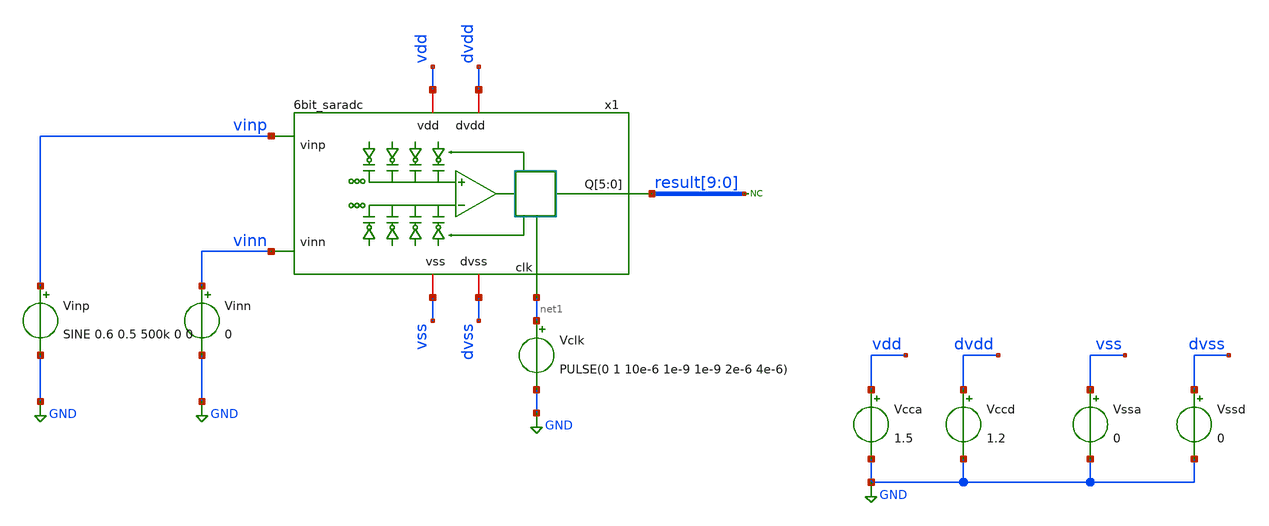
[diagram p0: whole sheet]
** sch_path: xschem/adc/tb_adc.sch
**.subckt tb_adc
x1 vdd vss dvdd dvss result[9] result[8] result[7] result[6] result[5] result[4] vinn net1 vinp
+ 6bit_saradc
Vclk net1 GND PULSE(0 1 10e-6 1e-9 1e-9 2e-6 4e-6)
Vssa vss GND 0
Vcca vdd GND 1.5
Vssd dvss GND 0
Vccd dvdd GND 1.2
Vinn vinn GND 0
Vinp vinp GND SINE 0.6 0.5 500k 0 0
* noconn result[9:0]
**** begin user architecture code

.lib $::SKYWATER_MODELS/models/sky130.lib.spice tt
.include $::SKYWATER_STDCELLS/cells/inv/sky130_fd_sc_hd__inv_4.spice
.include $::SKYWATER_STDCELLS/cells/decap/sky130_fd_sc_hd__decap_8.spice
.include $::SKYWATER_STDCELLS/cells/decap/sky130_fd_sc_hd__decap_3.spice
.include $::SKYWATER_STDCELLS/cells/buf/sky130_fd_sc_hd__buf_1.spice
.include $::SKYWATER_STDCELLS/cells/inv/sky130_fd_sc_hd__inv_1.spice
.include $::SKYWATER_STDCELLS/cells/inv/sky130_fd_sc_hd__inv_2.spice
.include $::SKYWATER_STDCELLS/cells/nor2/sky130_fd_sc_hd__nor2_1.spice
.include $::SKYWATER_STDCELLS/cells/or3/sky130_fd_sc_hd__or3_1.spice
.include $::SKYWATER_STDCELLS/cells/and2/sky130_fd_sc_hd__and2_0.spice
.include $::SKYWATER_STDCELLS/cells/dfrbp/sky130_fd_sc_hd__dfrbp_1.spice
.include $::SKYWATER_STDCELLS/cells/tap/sky130_fd_sc_hd__tap_2.spice

 *-------------------------
* normal setup
*-------------------------
.options method = gear
.options gmin   = 1e-15
.options abstol = 1e-14
.options chtol  = 1e-18
.options reltol = 100e-6
*-------------------------

*-------------------------
* extracted logic setup
*-------------------------
*.options method = gear
*.options gmin   = 1e-12
*.options abstol = 1e-10
*.options chtol  = 1e-12
*.options reltol = 100e-3
*-------------------------



*.include $::DESIGN_PATH/switches/bootstrapped_sw.sp
*.include $::DESIGN_PATH/sar_10b/dac/dac_mom.pex.sp
*.include $::DESIGN_PATH/sar_10b/sar/sar.pex.spice
*.include $::DESIGN_PATH/sar_10b/sar/sar_mom.pex.spice
*.include $::DESIGN_PATH/sar_10b/sar/sar_mim.pex.spice
*.include $::DESIGN_PATH/sar_10b/control/sarlogic.ext.spice
*.include $::DESIGN_PATH/sar_10b/sar/sar.pex.spice
*.include $::DESIGN_PATH/sar_10b/sar/sar.ext.spice

.param MC_SWITCH=0
.param vin=0.1
.param vcm=0.75
.param vsigp=vcm + vin/2
.param vsign=vcm - vin/2

.tran 100e-9 10e-6 uic

.control

run

.endc

 * FET CORNERS
*.include $::SKYWATER_MODELS/corners/tt_all.spice
*.include $::SKYWATER_MODELS/corners/ff_all.spice
*.include $::SKYWATER_MODELS/corners/ss_all.spice
*.include $::SKYWATER_MODELS/corners/tt.spice
*.include $::SKYWATER_MODELS/corners/ff.spice
*.include $::SKYWATER_MODELS/corners/ss.spice
*.include $::SKYWATER_MODELS/corners/sf.spice
*.include $::SKYWATER_MODELS/corners/fs.spice

* TT + R + C
*.include $::SKYWATER_MODELS/corners/tt_rmax_cmax.spice
*.include $::SKYWATER_MODELS/corners/tt_rmin_cmin.spice
*.include $::SKYWATER_MODELS/corners/tt_rmax_cmin.spice
*.include $::SKYWATER_MODELS/corners/tt_rmin_cmax.spice

* FF + R + C
*.include $::SKYWATER_MODELS/corners/ff_rmax_cmax.spice
*.include $::SKYWATER_MODELS/corners/ff_rmin_cmin.spice
*.include $::SKYWATER_MODELS/corners/ff_rmax_cmin.spice
*.include $::SKYWATER_MODELS/corners/ff_rmin_cmax.spice


* SS + R + C
*.include $::SKYWATER_MODELS/corners/ss_rmax_cmax.spice
*.include $::SKYWATER_MODELS/corners/ss_rmin_cmin.spice
*.include $::SKYWATER_MODELS/corners/ss_rmax_cmin.spice
*.include $::SKYWATER_MODELS/corners/ss_rmin_cmax.spice

* SF + R + C
*.include $::SKYWATER_MODELS/corners/sf_rmax_cmax.spice
*.include $::SKYWATER_MODELS/corners/sf_rmin_cmin.spice
*.include $::SKYWATER_MODELS/corners/sf_rmax_cmin.spice
*.include $::SKYWATER_MODELS/corners/sf_rmin_cmax.spice

* FS + R + C
*.include $::SKYWATER_MODELS/corners/fs_rmax_cmax.spice
*.include $::SKYWATER_MODELS/corners/fs_rmin_cmin.spice
*.include $::SKYWATER_MODELS/corners/fs_rmax_cmin.spice
*.include $::SKYWATER_MODELS/corners/fs_rmin_cmax.spice

**** end user architecture code
**.ends
.GLOBAL GND
.end
